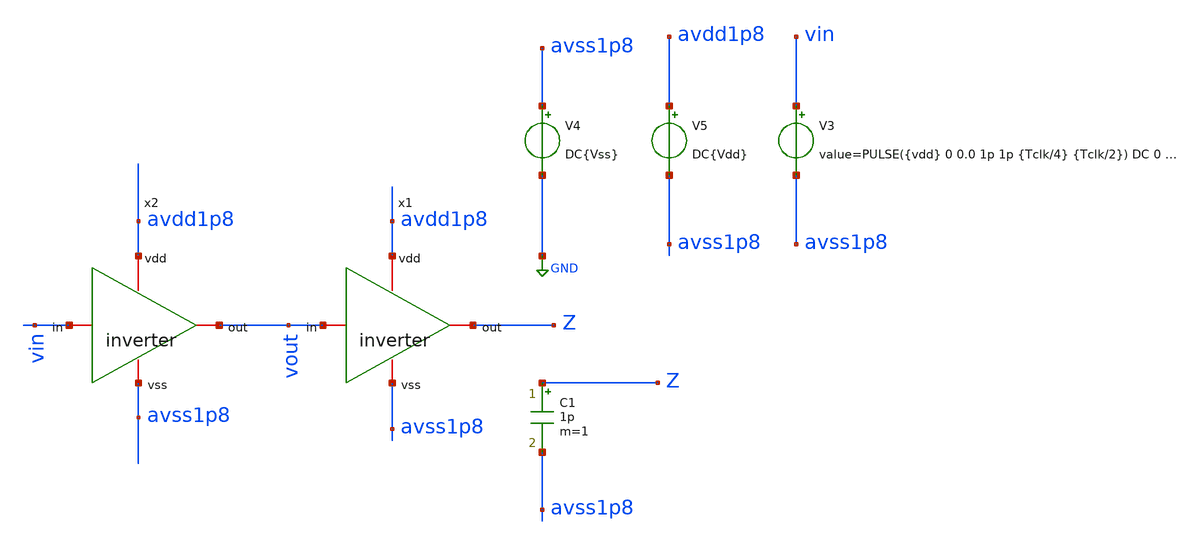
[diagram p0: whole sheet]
** sch_path: tstbnch/tb_inverter.sch
**.subckt tb_inverter
V4 avss1p8 GND DC{Vss}
V5 avdd1p8 avss1p8 DC{Vdd}
V3 vin avss1p8 PULSE({vdd} 0 0.0 1p 1p {Tclk/4} {Tclk/2}) DC 0 AC 0
C1 Z avss1p8 1p m=1
x1 avdd1p8 vout Z avss1p8 inverter
x2 avdd1p8 vin vout avss1p8 inverter
**** begin user architecture code


* Circuit Parameters
.param vdd = 1.8
.param vss = 0.0
.param Tclk = 10n
.options TEMP = 65.0
* Include Models
.lib /foss/pdks/sky130A/libs.tech/ngspice/sky130.lib.spice TT
* OP Parameters & Singals to save
.save all
*Simulations
.control
tran 0.01u 100n
setplot tran1
plot v(vin) v(vout)+2
reset
dc V6 0 1.8 0.01
setplot dc
plot vin vout ylabel vout xlabel vin
set filetype = ascii
write dcsweep.raw
.endc

.end


**** end user architecture code
**.ends

* expanding   symbol:  /foss/designs/sch/inverter.sym # of pins=4
** sym_path: sch/inverter.sym
** sch_path: sch/inverter.sch
.subckt inverter vdd in out vss
*.iopin out
*.iopin vdd
*.iopin vss
*.iopin in
XM1 out in vss vss sky130_fd_pr__nfet_01v8 L=0.15 W=0.45 nf=1 ad='int((nf+1)/2) * W/nf * 0.29' as='int((nf+2)/2) * W/nf * 0.29'
+ pd='2*int((nf+1)/2) * (W/nf + 0.29)' ps='2*int((nf+2)/2) * (W/nf + 0.29)' nrd='0.29 / W' nrs='0.29 / W'
+ sa=0 sb=0 sd=0 mult=1 m=1
XM2 out in vdd vdd sky130_fd_pr__pfet_01v8 L=0.15 W=0.45 nf=1 ad='int((nf+1)/2) * W/nf * 0.29' as='int((nf+2)/2) * W/nf * 0.29'
+ pd='2*int((nf+1)/2) * (W/nf + 0.29)' ps='2*int((nf+2)/2) * (W/nf + 0.29)' nrd='0.29 / W' nrs='0.29 / W'
+ sa=0 sb=0 sd=0 mult=1 m=1
.ends

.GLOBAL GND
.end
